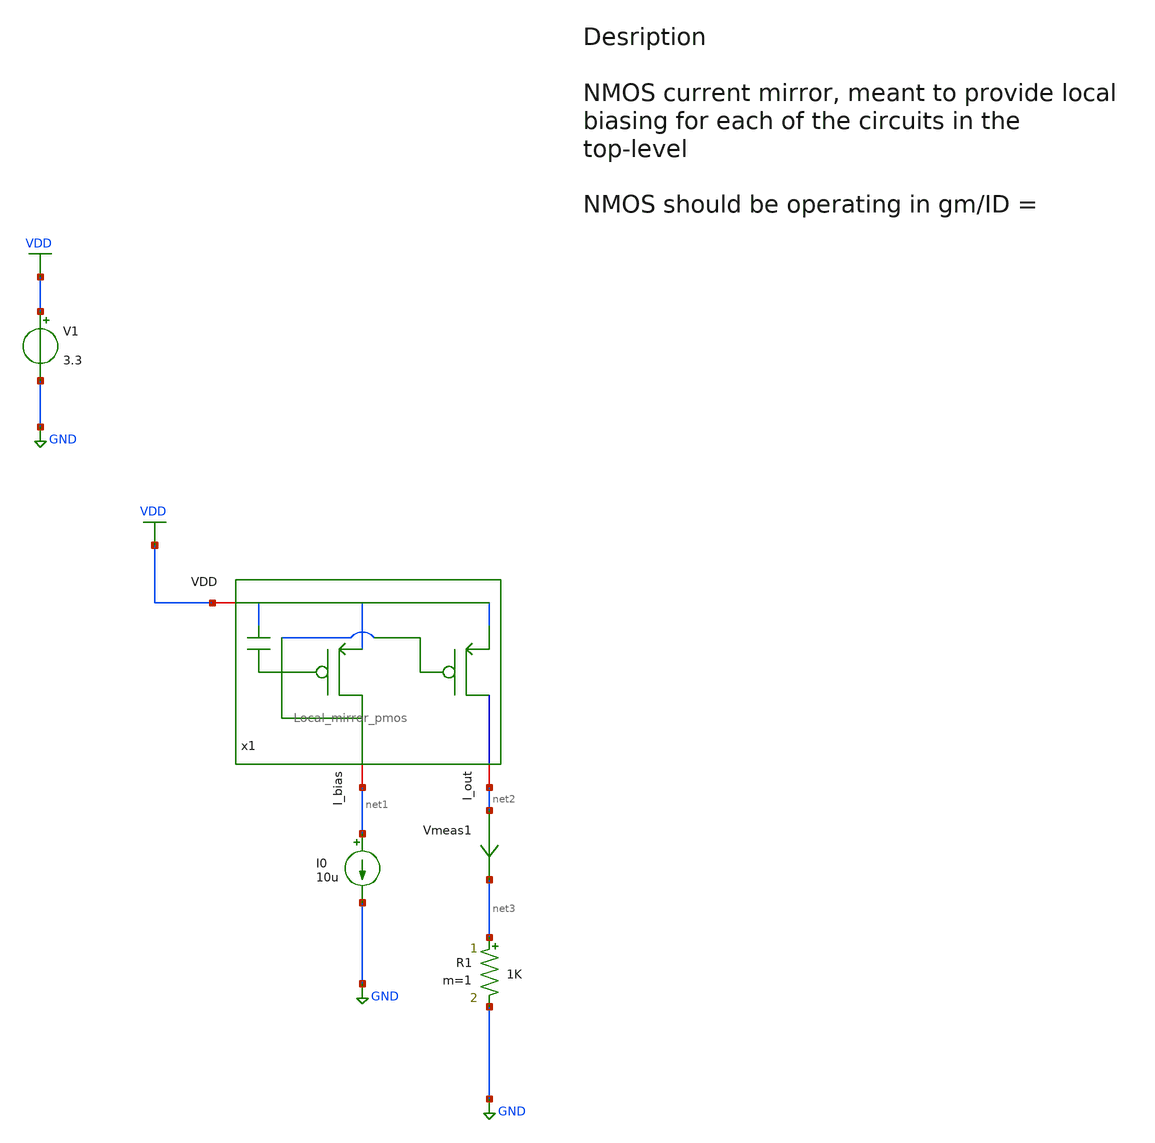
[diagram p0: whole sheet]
** sch_path: src/design_tb/Local_mirror_pmos_tb.sch
**.subckt Local_mirror_pmos_tb
I0 net1 GND 10u
V1 VDD GND 3.3
.save i(v1)
Vmeas1 net2 net3 0
.save i(vmeas1)
R1 net3 GND 1K m=1
x1 VDD net2 net1 Local_mirror_pmos l_ref=0.4 w_ref=2 l_mir=0.4 w_mir=6
**** begin user architecture code

.include $::180MCU_MODELS/design.ngspice
.lib $::180MCU_MODELS/sm141064.ngspice typical
.lib $::180MCU_MODELS/sm141064.ngspice mimcap_typical
.lib $::180MCU_MODELS/sm141064.ngspice cap_mim
.lib $::180MCU_MODELS/sm141064.ngspice res_typical
.lib $::180MCU_MODELS/sm141064.ngspice diode_typical



* Add convergence aids
.option method=gear

.control

    * operating point
    op
    show

    write Local_mirror_pmos_tb.raw

    set appendwrite

    * Transient analysis to observe mixing operation
    tran 1n 0.01u
    write Local_mirror_pmos_tb.raw

.endc


**** end user architecture code
**.ends

* expanding   symbol:  /home/vasil/Downloads/SSCS_PICO_2025/src/design_xsch/Local_mirror_pmos.sym #
*+ of pins=3
** sym_path: src/design_xsch/Local_mirror_pmos.sym
** sch_path: src/design_xsch/Local_mirror_pmos.sch
.subckt Local_mirror_pmos VDD I_out I_BIAS   l_ref=0.28u w_ref=0.22u   l_mir=0.28u w_mir=0.22u
*.iopin I_BIAS
*.iopin VDD
*.iopin I_out
XM1 I_BIAS I_BIAS VDD VDD pfet_03v3 L=l_ref W=w_ref nf=1 ad='int((nf+1)/2) * W/nf * 0.18u' as='int((nf+2)/2) * W/nf * 0.18u'
+ pd='2*int((nf+1)/2) * (W/nf + 0.18u)' ps='2*int((nf+2)/2) * (W/nf + 0.18u)' nrd='0.18u / W' nrs='0.18u / W'
+ sa=0 sb=0 sd=0 m=1
XM2 I_out I_BIAS VDD VDD pfet_03v3 L=l_mir W=w_mir nf=1 ad='int((nf+1)/2) * W/nf * 0.18u' as='int((nf+2)/2) * W/nf * 0.18u'
+ pd='2*int((nf+1)/2) * (W/nf + 0.18u)' ps='2*int((nf+2)/2) * (W/nf + 0.18u)' nrd='0.18u / W' nrs='0.18u / W'
+ sa=0 sb=0 sd=0 m=1
XC1 VDD I_BIAS cap_mim_1f0fF c_width=1e-6 c_length=1e-6 m=1
.ends

.GLOBAL GND
.GLOBAL VDD
.end
